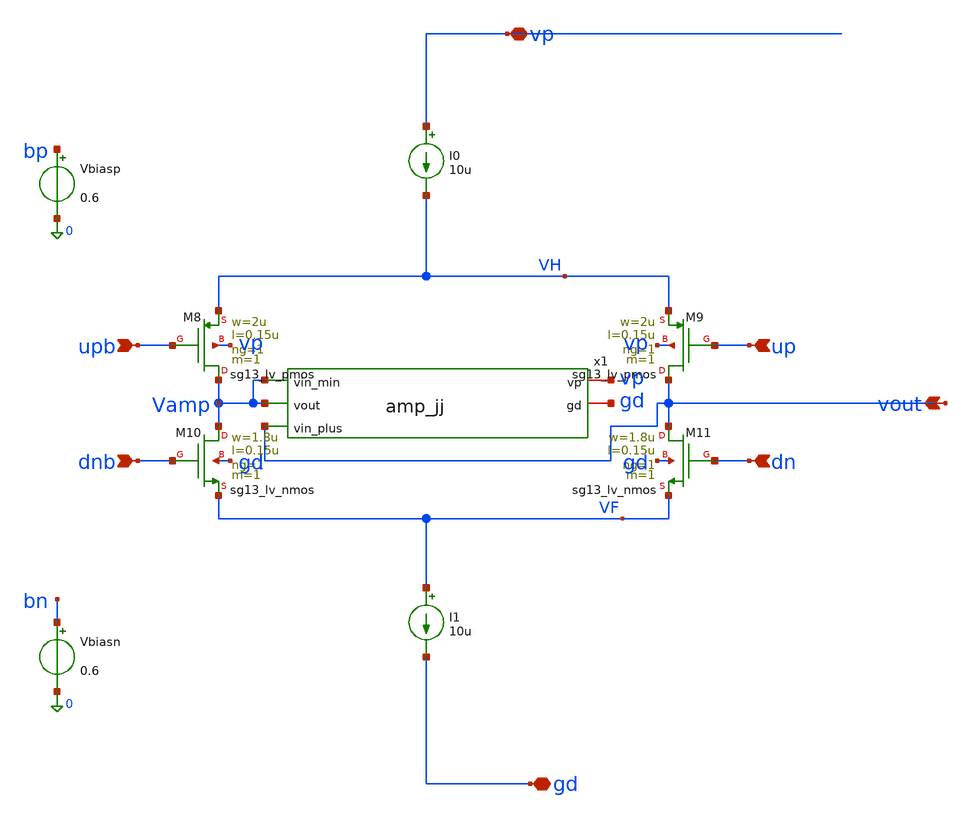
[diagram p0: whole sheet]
** sch_path: charge_pump/cp_v1_no_mirror.sch
**.subckt cp_v1_no_mirror upb dnb up dn vp gd vout
*.ipin upb
*.ipin dnb
*.ipin up
*.ipin dn
*.iopin vp
*.iopin gd
*.opin vout
XM8 Vamp upb VH vp sg13_lv_pmos w=2u l=0.15u ng=1 m=1 mm_ok=1
XM9 vout up VH vp sg13_lv_pmos w=2u l=0.15u ng=1 m=1 mm_ok=1
XM10 Vamp dnb VF gd sg13_lv_nmos w=1.8u l=0.15u ng=1 m=1 mm_ok=1
XM11 vout dn VF gd sg13_lv_nmos w=1.8u l=0.15u ng=1 m=1 mm_ok=1
x1 vp Vamp Vamp vout gd amp_jj
Vbiasp bp 0 0.6
Vbiasn bn 0 0.6
I0 vp VH 10u
I1 VF gd 10u
**.ends
.end
